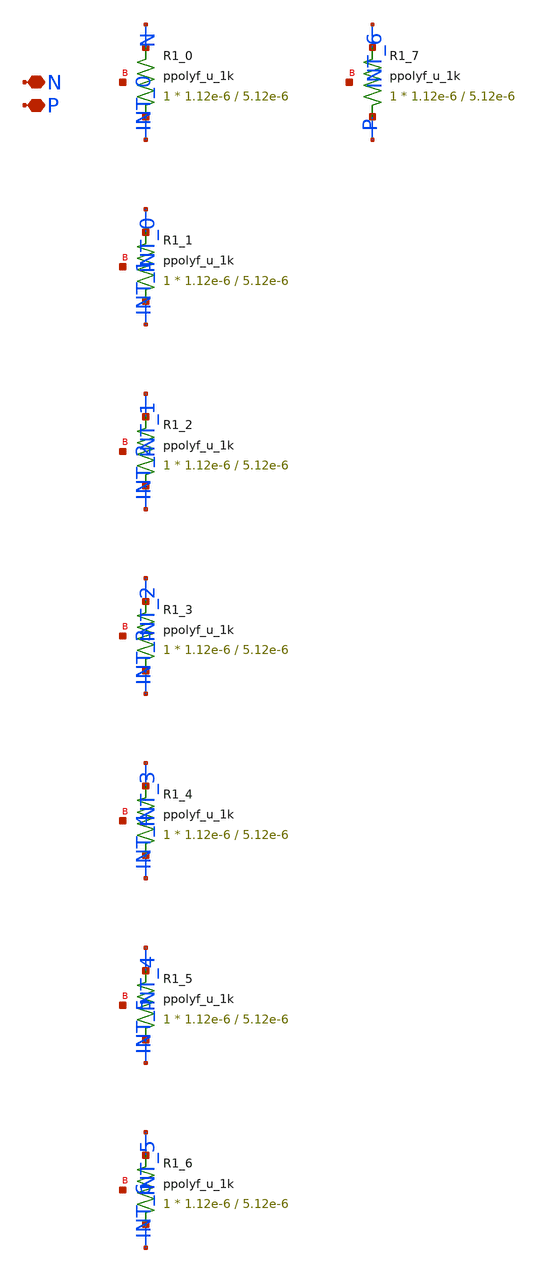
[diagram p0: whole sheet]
** sch_path: design/LELO_TR_GF180MCUD/LELOTR_RES8.sch
**.subckt LELOTR_RES8 N P
*.iopin N
*.iopin P
XR1_0 INT_0 N net1 ppolyf_u_1k r_width=1.12e-6 r_length=5.12e-6 m=1
XR1_1 INT_1 INT_0 net2 ppolyf_u_1k r_width=1.12e-6 r_length=5.12e-6 m=1
XR1_2 INT_2 INT_1 net3 ppolyf_u_1k r_width=1.12e-6 r_length=5.12e-6 m=1
XR1_3 INT_3 INT_2 net4 ppolyf_u_1k r_width=1.12e-6 r_length=5.12e-6 m=1
XR1_4 INT_4 INT_3 net5 ppolyf_u_1k r_width=1.12e-6 r_length=5.12e-6 m=1
XR1_5 INT_5 INT_4 net6 ppolyf_u_1k r_width=1.12e-6 r_length=5.12e-6 m=1
XR1_6 INT_6 INT_5 net7 ppolyf_u_1k r_width=1.12e-6 r_length=5.12e-6 m=1
XR1_7 P INT_6 net8 ppolyf_u_1k r_width=1.12e-6 r_length=5.12e-6 m=1
**.ends
.end
